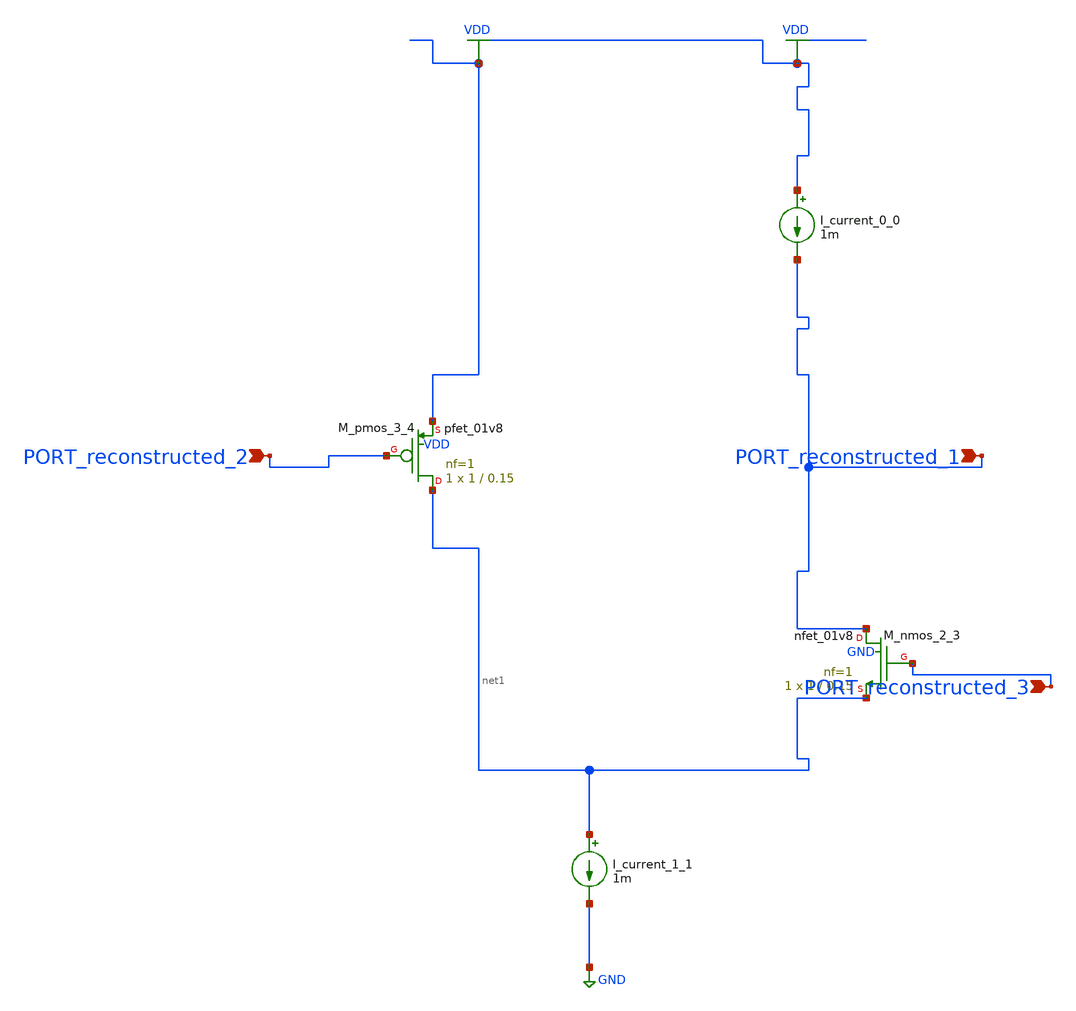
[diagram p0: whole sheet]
** sch_path: schematics/AMSNet/633.sch
**.subckt 633 PORT_reconstructed_3 PORT_reconstructed_1 PORT_reconstructed_2
*.ipin PORT_reconstructed_3
*.ipin PORT_reconstructed_1
*.ipin PORT_reconstructed_2
I_current_0_0 VDD PORT_reconstructed_1 1m
I_current_1_1 net1 GND 1m
XM_nmos_2_3 PORT_reconstructed_1 PORT_reconstructed_3 net1 GND sky130_fd_pr__nfet_01v8 L=0.15 W=1 nf=1
+ ad='int((1 + 1)/2) * 1 / 1 * 0.29' as='int((1 + 2)/2) * 1 / 1 * 0.29' pd='2*int((1 + 1)/2) * (1 / 1 + 0.29)'
+ ps='2*int((1 + 2)/2) * (1 / 1 + 0.29)' nrd='0.29 / 1 ' nrs='0.29 / 1 ' sa=0 sb=0 sd=0 mult=1 m=1
XM_pmos_3_4 net1 PORT_reconstructed_2 VDD VDD sky130_fd_pr__pfet_01v8 L=0.15 W=1 nf=1 ad='int((1 + 1)/2) * 1 / 1 * 0.29'
+ as='int((1 + 2)/2) * 1 / 1 * 0.29' pd='2*int((1 + 1)/2) * (1 / 1 + 0.29)' ps='2*int((1 + 2)/2) * (1 / 1 + 0.29)'
+ nrd='0.29 / 1 ' nrs='0.29 / 1 ' sa=0 sb=0 sd=0 mult=1 m=1
**.ends
.GLOBAL GND
.GLOBAL VDD
.end
